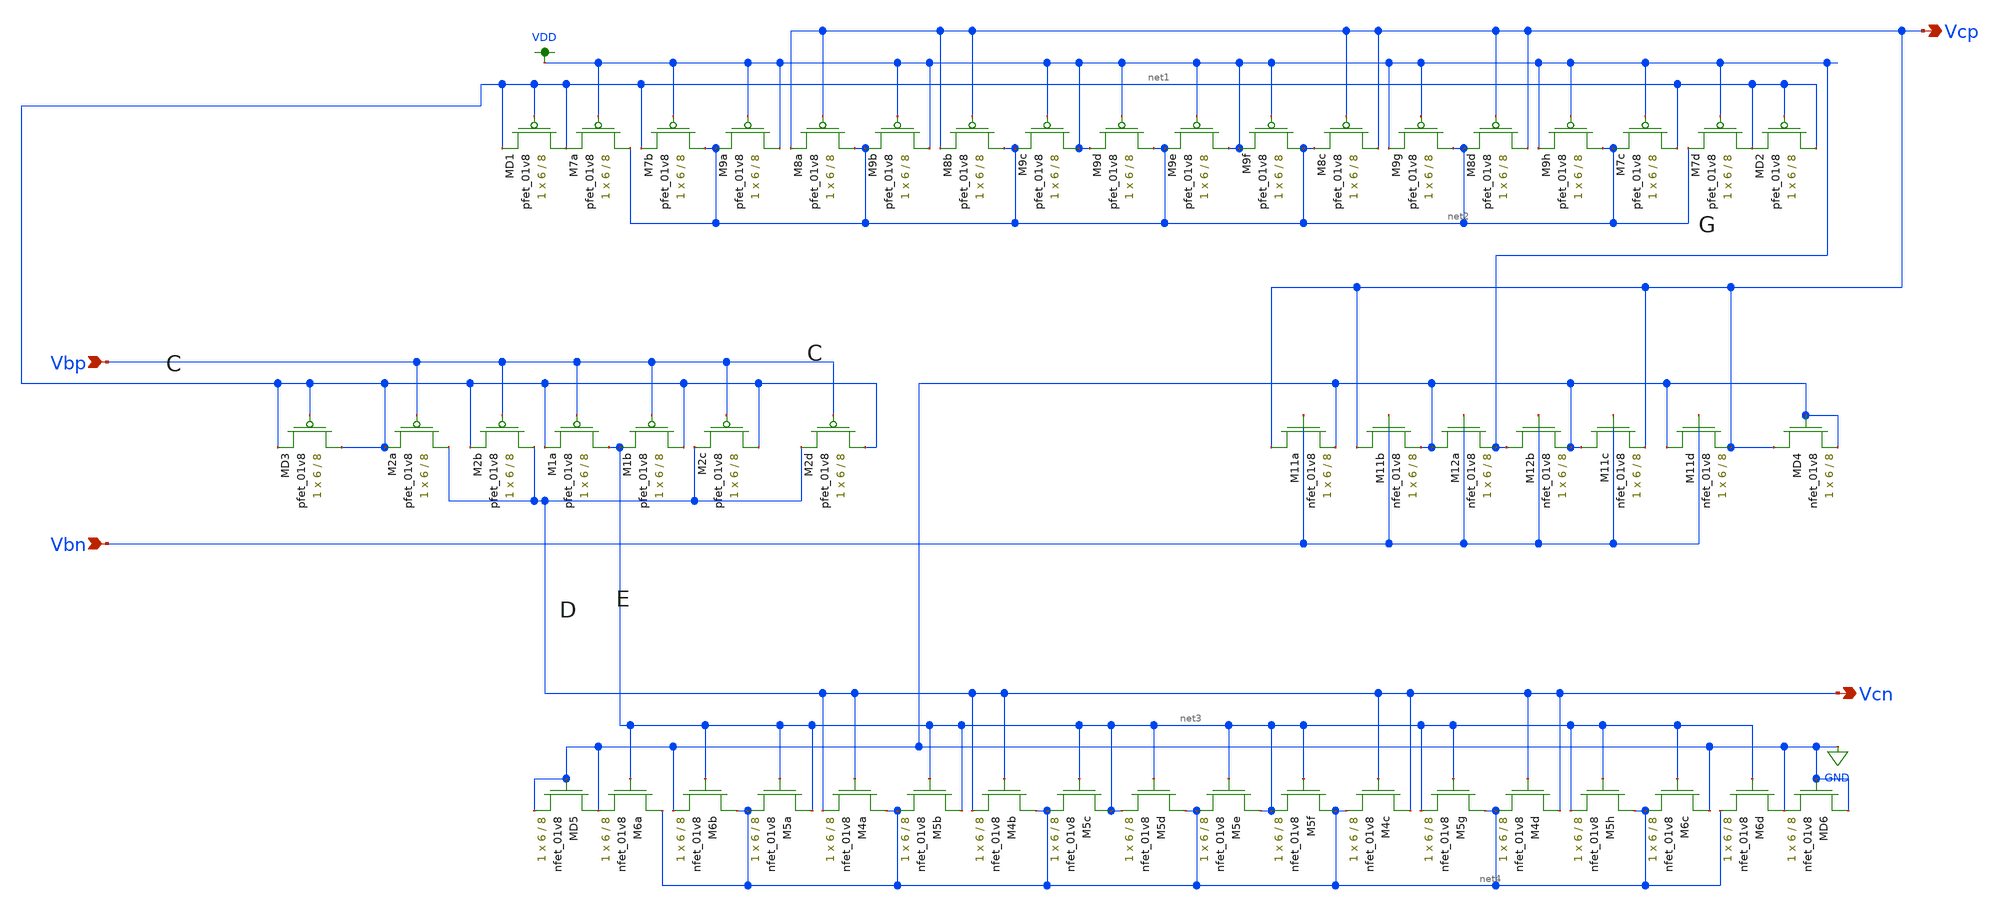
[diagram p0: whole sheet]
** sch_path: xschem/VGen.sch
**.subckt VGen Vbn Vbp Vcp Vcn
*.ipin Vbn
*.ipin Vbp
*.opin Vcp
*.opin Vcn
XMD2 net1 net1 net1 VDD sky130_fd_pr__pfet_01v8 L=8 W=6 nf=1 ad='int((nf+1)/2) * W/nf * 0.29' as='int((nf+2)/2) * W/nf * 0.29'
+ pd='2*int((nf+1)/2) * (W/nf + 0.29)' ps='2*int((nf+2)/2) * (W/nf + 0.29)' nrd='0.29 / W' nrs='0.29 / W'
+ sa=0 sb=0 sd=0 mult=1 m=1
XM7d net1 VDD net2 VDD sky130_fd_pr__pfet_01v8 L=8 W=6 nf=1 ad='int((nf+1)/2) * W/nf * 0.29' as='int((nf+2)/2) * W/nf * 0.29'
+ pd='2*int((nf+1)/2) * (W/nf + 0.29)' ps='2*int((nf+2)/2) * (W/nf + 0.29)' nrd='0.29 / W' nrs='0.29 / W'
+ sa=0 sb=0 sd=0 mult=1 m=1
XM7c net1 VDD net2 VDD sky130_fd_pr__pfet_01v8 L=8 W=6 nf=1 ad='int((nf+1)/2) * W/nf * 0.29' as='int((nf+2)/2) * W/nf * 0.29'
+ pd='2*int((nf+1)/2) * (W/nf + 0.29)' ps='2*int((nf+2)/2) * (W/nf + 0.29)' nrd='0.29 / W' nrs='0.29 / W'
+ sa=0 sb=0 sd=0 mult=1 m=1
XM9h net2 VDD VDD VDD sky130_fd_pr__pfet_01v8 L=8 W=6 nf=1 ad='int((nf+1)/2) * W/nf * 0.29' as='int((nf+2)/2) * W/nf * 0.29'
+ pd='2*int((nf+1)/2) * (W/nf + 0.29)' ps='2*int((nf+2)/2) * (W/nf + 0.29)' nrd='0.29 / W' nrs='0.29 / W'
+ sa=0 sb=0 sd=0 mult=1 m=1
XM9f net2 VDD VDD VDD sky130_fd_pr__pfet_01v8 L=8 W=6 nf=1 ad='int((nf+1)/2) * W/nf * 0.29' as='int((nf+2)/2) * W/nf * 0.29'
+ pd='2*int((nf+1)/2) * (W/nf + 0.29)' ps='2*int((nf+2)/2) * (W/nf + 0.29)' nrd='0.29 / W' nrs='0.29 / W'
+ sa=0 sb=0 sd=0 mult=1 m=1
XM9e VDD VDD net2 VDD sky130_fd_pr__pfet_01v8 L=8 W=6 nf=1 ad='int((nf+1)/2) * W/nf * 0.29' as='int((nf+2)/2) * W/nf * 0.29'
+ pd='2*int((nf+1)/2) * (W/nf + 0.29)' ps='2*int((nf+2)/2) * (W/nf + 0.29)' nrd='0.29 / W' nrs='0.29 / W'
+ sa=0 sb=0 sd=0 mult=1 m=1
XM9d net2 VDD VDD VDD sky130_fd_pr__pfet_01v8 L=8 W=6 nf=1 ad='int((nf+1)/2) * W/nf * 0.29' as='int((nf+2)/2) * W/nf * 0.29'
+ pd='2*int((nf+1)/2) * (W/nf + 0.29)' ps='2*int((nf+2)/2) * (W/nf + 0.29)' nrd='0.29 / W' nrs='0.29 / W'
+ sa=0 sb=0 sd=0 mult=1 m=1
XM9b VDD VDD net2 VDD sky130_fd_pr__pfet_01v8 L=8 W=6 nf=1 ad='int((nf+1)/2) * W/nf * 0.29' as='int((nf+2)/2) * W/nf * 0.29'
+ pd='2*int((nf+1)/2) * (W/nf + 0.29)' ps='2*int((nf+2)/2) * (W/nf + 0.29)' nrd='0.29 / W' nrs='0.29 / W'
+ sa=0 sb=0 sd=0 mult=1 m=1
XM8a net2 Vcp Vcp VDD sky130_fd_pr__pfet_01v8 L=8 W=6 nf=1 ad='int((nf+1)/2) * W/nf * 0.29' as='int((nf+2)/2) * W/nf * 0.29'
+ pd='2*int((nf+1)/2) * (W/nf + 0.29)' ps='2*int((nf+2)/2) * (W/nf + 0.29)' nrd='0.29 / W' nrs='0.29 / W'
+ sa=0 sb=0 sd=0 mult=1 m=1
XM9a VDD VDD net2 VDD sky130_fd_pr__pfet_01v8 L=8 W=6 nf=1 ad='int((nf+1)/2) * W/nf * 0.29' as='int((nf+2)/2) * W/nf * 0.29'
+ pd='2*int((nf+1)/2) * (W/nf + 0.29)' ps='2*int((nf+2)/2) * (W/nf + 0.29)' nrd='0.29 / W' nrs='0.29 / W'
+ sa=0 sb=0 sd=0 mult=1 m=1
XM7b net2 VDD net1 VDD sky130_fd_pr__pfet_01v8 L=8 W=6 nf=1 ad='int((nf+1)/2) * W/nf * 0.29' as='int((nf+2)/2) * W/nf * 0.29'
+ pd='2*int((nf+1)/2) * (W/nf + 0.29)' ps='2*int((nf+2)/2) * (W/nf + 0.29)' nrd='0.29 / W' nrs='0.29 / W'
+ sa=0 sb=0 sd=0 mult=1 m=1
XM7a net2 VDD net1 VDD sky130_fd_pr__pfet_01v8 L=8 W=6 nf=1 ad='int((nf+1)/2) * W/nf * 0.29' as='int((nf+2)/2) * W/nf * 0.29'
+ pd='2*int((nf+1)/2) * (W/nf + 0.29)' ps='2*int((nf+2)/2) * (W/nf + 0.29)' nrd='0.29 / W' nrs='0.29 / W'
+ sa=0 sb=0 sd=0 mult=1 m=1
XMD1 net1 net1 net1 VDD sky130_fd_pr__pfet_01v8 L=8 W=6 nf=1 ad='int((nf+1)/2) * W/nf * 0.29' as='int((nf+2)/2) * W/nf * 0.29'
+ pd='2*int((nf+1)/2) * (W/nf + 0.29)' ps='2*int((nf+2)/2) * (W/nf + 0.29)' nrd='0.29 / W' nrs='0.29 / W'
+ sa=0 sb=0 sd=0 mult=1 m=1
XM2d net1 Vbp Vcn VDD sky130_fd_pr__pfet_01v8 L=8 W=6 nf=1 ad='int((nf+1)/2) * W/nf * 0.29' as='int((nf+2)/2) * W/nf * 0.29'
+ pd='2*int((nf+1)/2) * (W/nf + 0.29)' ps='2*int((nf+2)/2) * (W/nf + 0.29)' nrd='0.29 / W' nrs='0.29 / W'
+ sa=0 sb=0 sd=0 mult=1 m=1
XM2c net1 Vbp Vcn VDD sky130_fd_pr__pfet_01v8 L=8 W=6 nf=1 ad='int((nf+1)/2) * W/nf * 0.29' as='int((nf+2)/2) * W/nf * 0.29'
+ pd='2*int((nf+1)/2) * (W/nf + 0.29)' ps='2*int((nf+2)/2) * (W/nf + 0.29)' nrd='0.29 / W' nrs='0.29 / W'
+ sa=0 sb=0 sd=0 mult=1 m=1
XM1b net1 Vbp net3 VDD sky130_fd_pr__pfet_01v8 L=8 W=6 nf=1 ad='int((nf+1)/2) * W/nf * 0.29' as='int((nf+2)/2) * W/nf * 0.29'
+ pd='2*int((nf+1)/2) * (W/nf + 0.29)' ps='2*int((nf+2)/2) * (W/nf + 0.29)' nrd='0.29 / W' nrs='0.29 / W'
+ sa=0 sb=0 sd=0 mult=1 m=1
XM1a net3 Vbp net1 VDD sky130_fd_pr__pfet_01v8 L=8 W=6 nf=1 ad='int((nf+1)/2) * W/nf * 0.29' as='int((nf+2)/2) * W/nf * 0.29'
+ pd='2*int((nf+1)/2) * (W/nf + 0.29)' ps='2*int((nf+2)/2) * (W/nf + 0.29)' nrd='0.29 / W' nrs='0.29 / W'
+ sa=0 sb=0 sd=0 mult=1 m=1
XM2b Vcn Vbp net1 VDD sky130_fd_pr__pfet_01v8 L=8 W=6 nf=1 ad='int((nf+1)/2) * W/nf * 0.29' as='int((nf+2)/2) * W/nf * 0.29'
+ pd='2*int((nf+1)/2) * (W/nf + 0.29)' ps='2*int((nf+2)/2) * (W/nf + 0.29)' nrd='0.29 / W' nrs='0.29 / W'
+ sa=0 sb=0 sd=0 mult=1 m=1
XM2a Vcn Vbp net1 VDD sky130_fd_pr__pfet_01v8 L=8 W=6 nf=1 ad='int((nf+1)/2) * W/nf * 0.29' as='int((nf+2)/2) * W/nf * 0.29'
+ pd='2*int((nf+1)/2) * (W/nf + 0.29)' ps='2*int((nf+2)/2) * (W/nf + 0.29)' nrd='0.29 / W' nrs='0.29 / W'
+ sa=0 sb=0 sd=0 mult=1 m=1
XM11d GND Vbn Vcp GND sky130_fd_pr__nfet_01v8 L=8 W=6 nf=1 ad='int((nf+1)/2) * W/nf * 0.29' as='int((nf+2)/2) * W/nf * 0.29'
+ pd='2*int((nf+1)/2) * (W/nf + 0.29)' ps='2*int((nf+2)/2) * (W/nf + 0.29)' nrd='0.29 / W' nrs='0.29 / W'
+ sa=0 sb=0 sd=0 mult=1 m=1
XM11c GND Vbn Vcp GND sky130_fd_pr__nfet_01v8 L=8 W=6 nf=1 ad='int((nf+1)/2) * W/nf * 0.29' as='int((nf+2)/2) * W/nf * 0.29'
+ pd='2*int((nf+1)/2) * (W/nf + 0.29)' ps='2*int((nf+2)/2) * (W/nf + 0.29)' nrd='0.29 / W' nrs='0.29 / W'
+ sa=0 sb=0 sd=0 mult=1 m=1
XM12b VDD Vbn GND GND sky130_fd_pr__nfet_01v8 L=8 W=6 nf=1 ad='int((nf+1)/2) * W/nf * 0.29' as='int((nf+2)/2) * W/nf * 0.29'
+ pd='2*int((nf+1)/2) * (W/nf + 0.29)' ps='2*int((nf+2)/2) * (W/nf + 0.29)' nrd='0.29 / W' nrs='0.29 / W'
+ sa=0 sb=0 sd=0 mult=1 m=1
XM12a GND Vbn VDD GND sky130_fd_pr__nfet_01v8 L=8 W=6 nf=1 ad='int((nf+1)/2) * W/nf * 0.29' as='int((nf+2)/2) * W/nf * 0.29'
+ pd='2*int((nf+1)/2) * (W/nf + 0.29)' ps='2*int((nf+2)/2) * (W/nf + 0.29)' nrd='0.29 / W' nrs='0.29 / W'
+ sa=0 sb=0 sd=0 mult=1 m=1
XM11b Vcp Vbn GND GND sky130_fd_pr__nfet_01v8 L=8 W=6 nf=1 ad='int((nf+1)/2) * W/nf * 0.29' as='int((nf+2)/2) * W/nf * 0.29'
+ pd='2*int((nf+1)/2) * (W/nf + 0.29)' ps='2*int((nf+2)/2) * (W/nf + 0.29)' nrd='0.29 / W' nrs='0.29 / W'
+ sa=0 sb=0 sd=0 mult=1 m=1
XM11a Vcp Vbn GND GND sky130_fd_pr__nfet_01v8 L=8 W=6 nf=1 ad='int((nf+1)/2) * W/nf * 0.29' as='int((nf+2)/2) * W/nf * 0.29'
+ pd='2*int((nf+1)/2) * (W/nf + 0.29)' ps='2*int((nf+2)/2) * (W/nf + 0.29)' nrd='0.29 / W' nrs='0.29 / W'
+ sa=0 sb=0 sd=0 mult=1 m=1
XMD4 Vcp GND GND GND sky130_fd_pr__nfet_01v8 L=8 W=6 nf=1 ad='int((nf+1)/2) * W/nf * 0.29' as='int((nf+2)/2) * W/nf * 0.29'
+ pd='2*int((nf+1)/2) * (W/nf + 0.29)' ps='2*int((nf+2)/2) * (W/nf + 0.29)' nrd='0.29 / W' nrs='0.29 / W'
+ sa=0 sb=0 sd=0 mult=1 m=1
XM9c VDD VDD net2 VDD sky130_fd_pr__pfet_01v8 L=8 W=6 nf=1 ad='int((nf+1)/2) * W/nf * 0.29' as='int((nf+2)/2) * W/nf * 0.29'
+ pd='2*int((nf+1)/2) * (W/nf + 0.29)' ps='2*int((nf+2)/2) * (W/nf + 0.29)' nrd='0.29 / W' nrs='0.29 / W'
+ sa=0 sb=0 sd=0 mult=1 m=1
XM8c Vcp Vcp net2 VDD sky130_fd_pr__pfet_01v8 L=8 W=6 nf=1 ad='int((nf+1)/2) * W/nf * 0.29' as='int((nf+2)/2) * W/nf * 0.29'
+ pd='2*int((nf+1)/2) * (W/nf + 0.29)' ps='2*int((nf+2)/2) * (W/nf + 0.29)' nrd='0.29 / W' nrs='0.29 / W'
+ sa=0 sb=0 sd=0 mult=1 m=1
XM8b net2 Vcp Vcp VDD sky130_fd_pr__pfet_01v8 L=8 W=6 nf=1 ad='int((nf+1)/2) * W/nf * 0.29' as='int((nf+2)/2) * W/nf * 0.29'
+ pd='2*int((nf+1)/2) * (W/nf + 0.29)' ps='2*int((nf+2)/2) * (W/nf + 0.29)' nrd='0.29 / W' nrs='0.29 / W'
+ sa=0 sb=0 sd=0 mult=1 m=1
XM9g net2 VDD VDD VDD sky130_fd_pr__pfet_01v8 L=8 W=6 nf=1 ad='int((nf+1)/2) * W/nf * 0.29' as='int((nf+2)/2) * W/nf * 0.29'
+ pd='2*int((nf+1)/2) * (W/nf + 0.29)' ps='2*int((nf+2)/2) * (W/nf + 0.29)' nrd='0.29 / W' nrs='0.29 / W'
+ sa=0 sb=0 sd=0 mult=1 m=1
XM8d Vcp Vcp net2 VDD sky130_fd_pr__pfet_01v8 L=8 W=6 nf=1 ad='int((nf+1)/2) * W/nf * 0.29' as='int((nf+2)/2) * W/nf * 0.29'
+ pd='2*int((nf+1)/2) * (W/nf + 0.29)' ps='2*int((nf+2)/2) * (W/nf + 0.29)' nrd='0.29 / W' nrs='0.29 / W'
+ sa=0 sb=0 sd=0 mult=1 m=1
XMD3 net1 net1 net1 VDD sky130_fd_pr__pfet_01v8 L=8 W=6 nf=1 ad='int((nf+1)/2) * W/nf * 0.29' as='int((nf+2)/2) * W/nf * 0.29'
+ pd='2*int((nf+1)/2) * (W/nf + 0.29)' ps='2*int((nf+2)/2) * (W/nf + 0.29)' nrd='0.29 / W' nrs='0.29 / W'
+ sa=0 sb=0 sd=0 mult=1 m=1
XM6a net4 net3 GND GND sky130_fd_pr__nfet_01v8 L=8 W=6 nf=1 ad='int((nf+1)/2) * W/nf * 0.29' as='int((nf+2)/2) * W/nf * 0.29'
+ pd='2*int((nf+1)/2) * (W/nf + 0.29)' ps='2*int((nf+2)/2) * (W/nf + 0.29)' nrd='0.29 / W' nrs='0.29 / W'
+ sa=0 sb=0 sd=0 mult=1 m=1
XM6b net4 net3 GND GND sky130_fd_pr__nfet_01v8 L=8 W=6 nf=1 ad='int((nf+1)/2) * W/nf * 0.29' as='int((nf+2)/2) * W/nf * 0.29'
+ pd='2*int((nf+1)/2) * (W/nf + 0.29)' ps='2*int((nf+2)/2) * (W/nf + 0.29)' nrd='0.29 / W' nrs='0.29 / W'
+ sa=0 sb=0 sd=0 mult=1 m=1
XM5a net3 net3 net4 GND sky130_fd_pr__nfet_01v8 L=8 W=6 nf=1 ad='int((nf+1)/2) * W/nf * 0.29' as='int((nf+2)/2) * W/nf * 0.29'
+ pd='2*int((nf+1)/2) * (W/nf + 0.29)' ps='2*int((nf+2)/2) * (W/nf + 0.29)' nrd='0.29 / W' nrs='0.29 / W'
+ sa=0 sb=0 sd=0 mult=1 m=1
XM4a net4 Vcn Vcn GND sky130_fd_pr__nfet_01v8 L=8 W=6 nf=1 ad='int((nf+1)/2) * W/nf * 0.29' as='int((nf+2)/2) * W/nf * 0.29'
+ pd='2*int((nf+1)/2) * (W/nf + 0.29)' ps='2*int((nf+2)/2) * (W/nf + 0.29)' nrd='0.29 / W' nrs='0.29 / W'
+ sa=0 sb=0 sd=0 mult=1 m=1
XM5b net3 net3 net4 GND sky130_fd_pr__nfet_01v8 L=8 W=6 nf=1 ad='int((nf+1)/2) * W/nf * 0.29' as='int((nf+2)/2) * W/nf * 0.29'
+ pd='2*int((nf+1)/2) * (W/nf + 0.29)' ps='2*int((nf+2)/2) * (W/nf + 0.29)' nrd='0.29 / W' nrs='0.29 / W'
+ sa=0 sb=0 sd=0 mult=1 m=1
XM5c net3 net3 net4 GND sky130_fd_pr__nfet_01v8 L=8 W=6 nf=1 ad='int((nf+1)/2) * W/nf * 0.29' as='int((nf+2)/2) * W/nf * 0.29'
+ pd='2*int((nf+1)/2) * (W/nf + 0.29)' ps='2*int((nf+2)/2) * (W/nf + 0.29)' nrd='0.29 / W' nrs='0.29 / W'
+ sa=0 sb=0 sd=0 mult=1 m=1
XM5d net4 net3 net3 GND sky130_fd_pr__nfet_01v8 L=8 W=6 nf=1 ad='int((nf+1)/2) * W/nf * 0.29' as='int((nf+2)/2) * W/nf * 0.29'
+ pd='2*int((nf+1)/2) * (W/nf + 0.29)' ps='2*int((nf+2)/2) * (W/nf + 0.29)' nrd='0.29 / W' nrs='0.29 / W'
+ sa=0 sb=0 sd=0 mult=1 m=1
XM4b net4 Vcn Vcn GND sky130_fd_pr__nfet_01v8 L=8 W=6 nf=1 ad='int((nf+1)/2) * W/nf * 0.29' as='int((nf+2)/2) * W/nf * 0.29'
+ pd='2*int((nf+1)/2) * (W/nf + 0.29)' ps='2*int((nf+2)/2) * (W/nf + 0.29)' nrd='0.29 / W' nrs='0.29 / W'
+ sa=0 sb=0 sd=0 mult=1 m=1
XM5e net3 net3 net4 GND sky130_fd_pr__nfet_01v8 L=8 W=6 nf=1 ad='int((nf+1)/2) * W/nf * 0.29' as='int((nf+2)/2) * W/nf * 0.29'
+ pd='2*int((nf+1)/2) * (W/nf + 0.29)' ps='2*int((nf+2)/2) * (W/nf + 0.29)' nrd='0.29 / W' nrs='0.29 / W'
+ sa=0 sb=0 sd=0 mult=1 m=1
XM5f net4 net3 net3 GND sky130_fd_pr__nfet_01v8 L=8 W=6 nf=1 ad='int((nf+1)/2) * W/nf * 0.29' as='int((nf+2)/2) * W/nf * 0.29'
+ pd='2*int((nf+1)/2) * (W/nf + 0.29)' ps='2*int((nf+2)/2) * (W/nf + 0.29)' nrd='0.29 / W' nrs='0.29 / W'
+ sa=0 sb=0 sd=0 mult=1 m=1
XM5g net4 net3 net3 GND sky130_fd_pr__nfet_01v8 L=8 W=6 nf=1 ad='int((nf+1)/2) * W/nf * 0.29' as='int((nf+2)/2) * W/nf * 0.29'
+ pd='2*int((nf+1)/2) * (W/nf + 0.29)' ps='2*int((nf+2)/2) * (W/nf + 0.29)' nrd='0.29 / W' nrs='0.29 / W'
+ sa=0 sb=0 sd=0 mult=1 m=1
XM4c Vcn Vcn net4 GND sky130_fd_pr__nfet_01v8 L=8 W=6 nf=1 ad='int((nf+1)/2) * W/nf * 0.29' as='int((nf+2)/2) * W/nf * 0.29'
+ pd='2*int((nf+1)/2) * (W/nf + 0.29)' ps='2*int((nf+2)/2) * (W/nf + 0.29)' nrd='0.29 / W' nrs='0.29 / W'
+ sa=0 sb=0 sd=0 mult=1 m=1
XM4d Vcn Vcn net4 GND sky130_fd_pr__nfet_01v8 L=8 W=6 nf=1 ad='int((nf+1)/2) * W/nf * 0.29' as='int((nf+2)/2) * W/nf * 0.29'
+ pd='2*int((nf+1)/2) * (W/nf + 0.29)' ps='2*int((nf+2)/2) * (W/nf + 0.29)' nrd='0.29 / W' nrs='0.29 / W'
+ sa=0 sb=0 sd=0 mult=1 m=1
XM5h net4 net3 net3 GND sky130_fd_pr__nfet_01v8 L=8 W=6 nf=1 ad='int((nf+1)/2) * W/nf * 0.29' as='int((nf+2)/2) * W/nf * 0.29'
+ pd='2*int((nf+1)/2) * (W/nf + 0.29)' ps='2*int((nf+2)/2) * (W/nf + 0.29)' nrd='0.29 / W' nrs='0.29 / W'
+ sa=0 sb=0 sd=0 mult=1 m=1
XM6c GND net3 net4 GND sky130_fd_pr__nfet_01v8 L=8 W=6 nf=1 ad='int((nf+1)/2) * W/nf * 0.29' as='int((nf+2)/2) * W/nf * 0.29'
+ pd='2*int((nf+1)/2) * (W/nf + 0.29)' ps='2*int((nf+2)/2) * (W/nf + 0.29)' nrd='0.29 / W' nrs='0.29 / W'
+ sa=0 sb=0 sd=0 mult=1 m=1
XM6d GND net3 net4 GND sky130_fd_pr__nfet_01v8 L=8 W=6 nf=1 ad='int((nf+1)/2) * W/nf * 0.29' as='int((nf+2)/2) * W/nf * 0.29'
+ pd='2*int((nf+1)/2) * (W/nf + 0.29)' ps='2*int((nf+2)/2) * (W/nf + 0.29)' nrd='0.29 / W' nrs='0.29 / W'
+ sa=0 sb=0 sd=0 mult=1 m=1
XMD6 GND GND GND GND sky130_fd_pr__nfet_01v8 L=8 W=6 nf=1 ad='int((nf+1)/2) * W/nf * 0.29' as='int((nf+2)/2) * W/nf * 0.29'
+ pd='2*int((nf+1)/2) * (W/nf + 0.29)' ps='2*int((nf+2)/2) * (W/nf + 0.29)' nrd='0.29 / W' nrs='0.29 / W'
+ sa=0 sb=0 sd=0 mult=1 m=1
XMD5 GND GND GND GND sky130_fd_pr__nfet_01v8 L=8 W=6 nf=1 ad='int((nf+1)/2) * W/nf * 0.29' as='int((nf+2)/2) * W/nf * 0.29'
+ pd='2*int((nf+1)/2) * (W/nf + 0.29)' ps='2*int((nf+2)/2) * (W/nf + 0.29)' nrd='0.29 / W' nrs='0.29 / W'
+ sa=0 sb=0 sd=0 mult=1 m=1
**.ends
.GLOBAL VDD
.GLOBAL GND
.end
